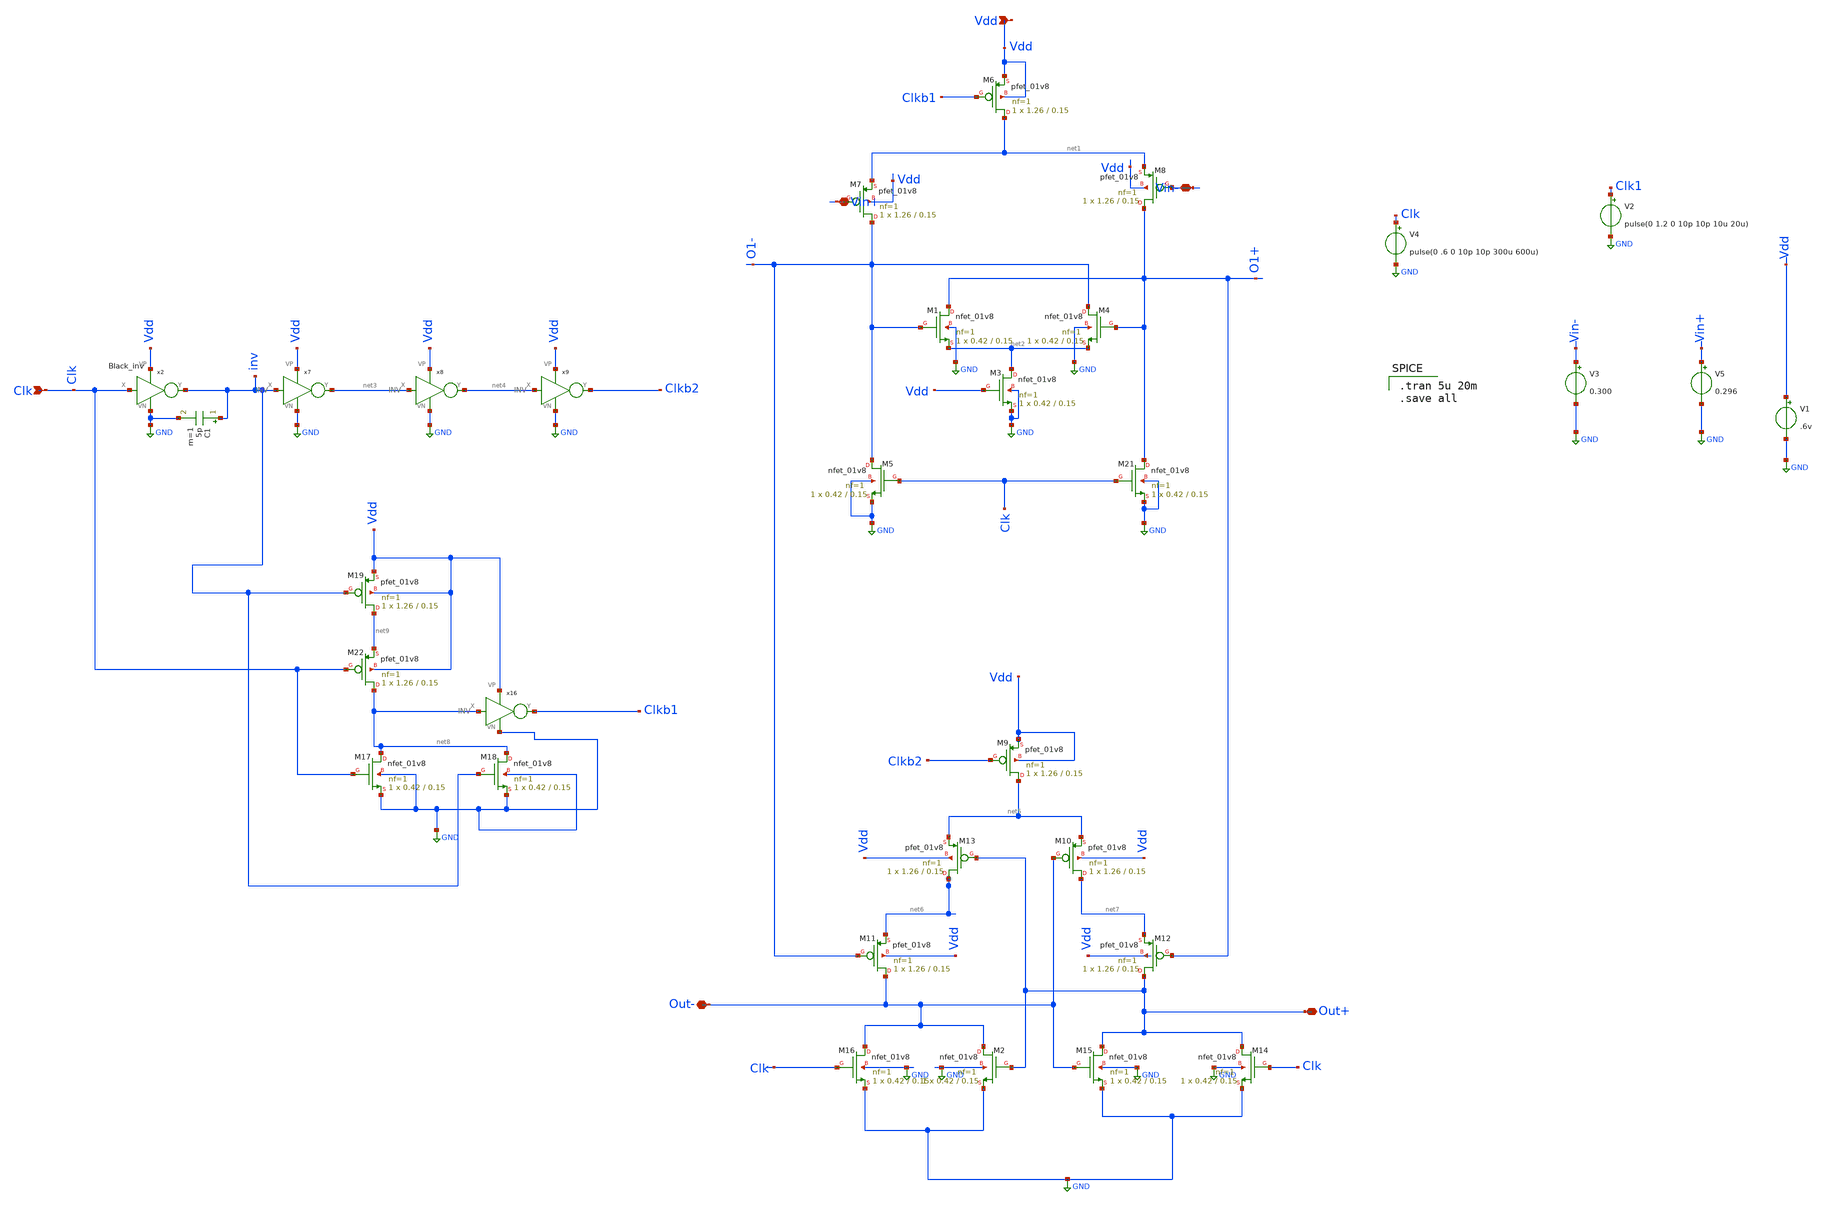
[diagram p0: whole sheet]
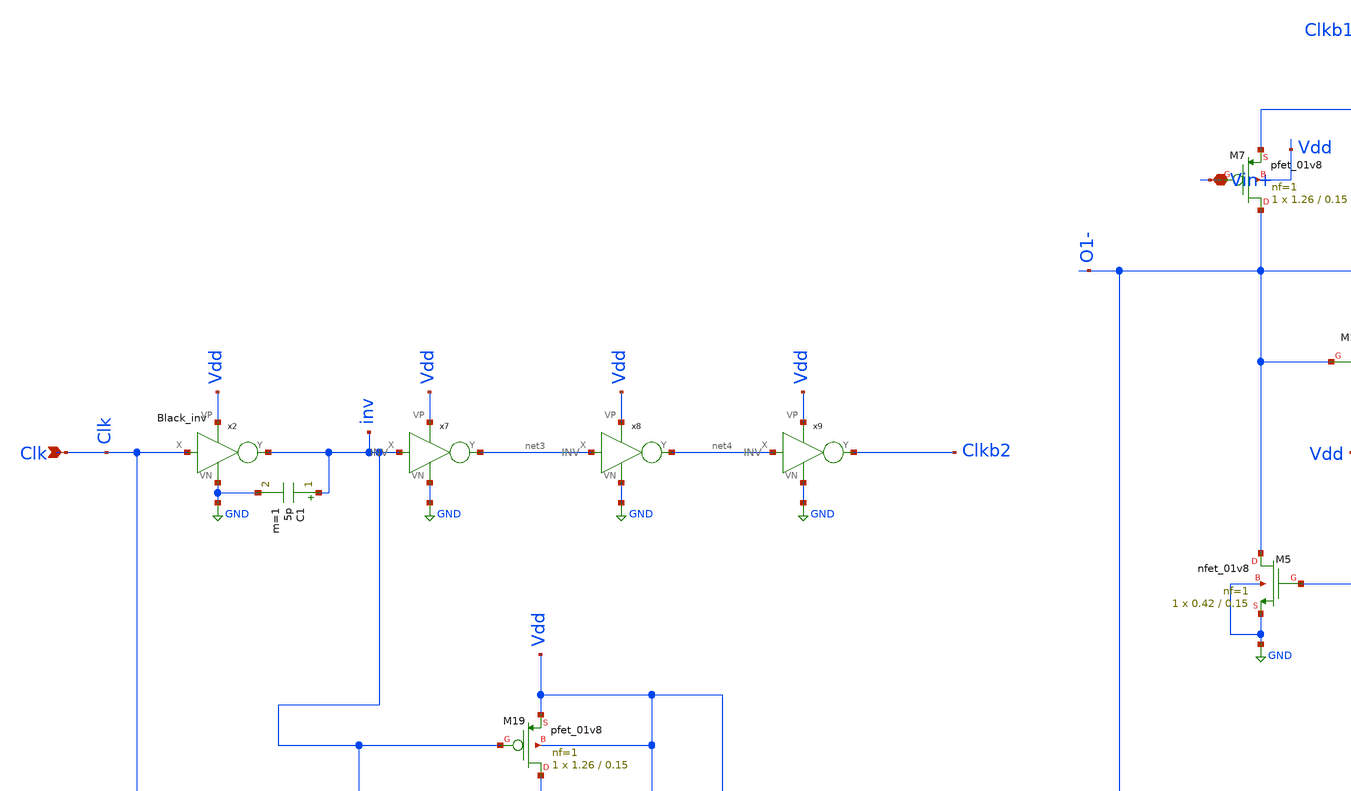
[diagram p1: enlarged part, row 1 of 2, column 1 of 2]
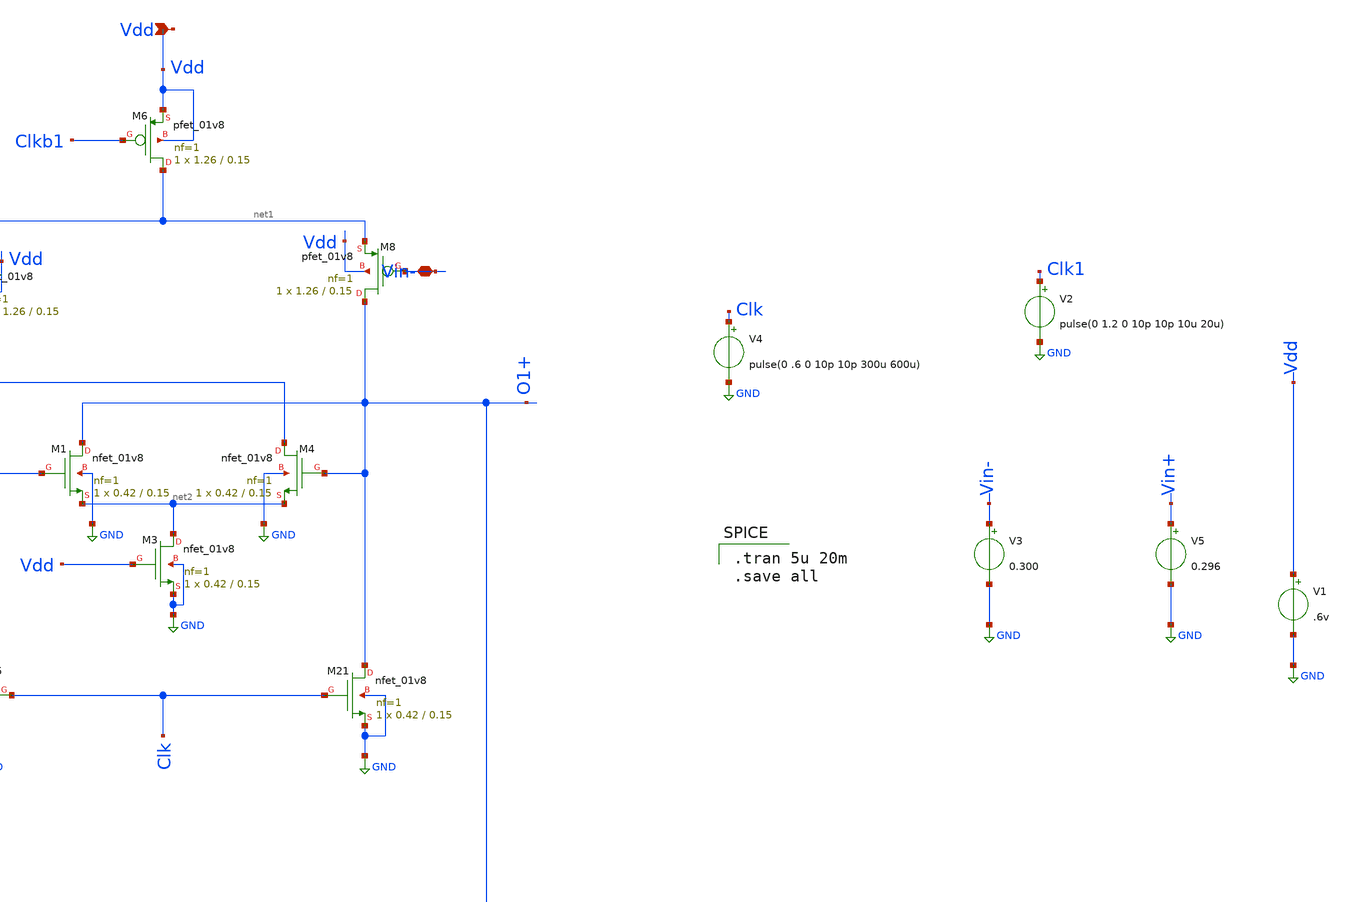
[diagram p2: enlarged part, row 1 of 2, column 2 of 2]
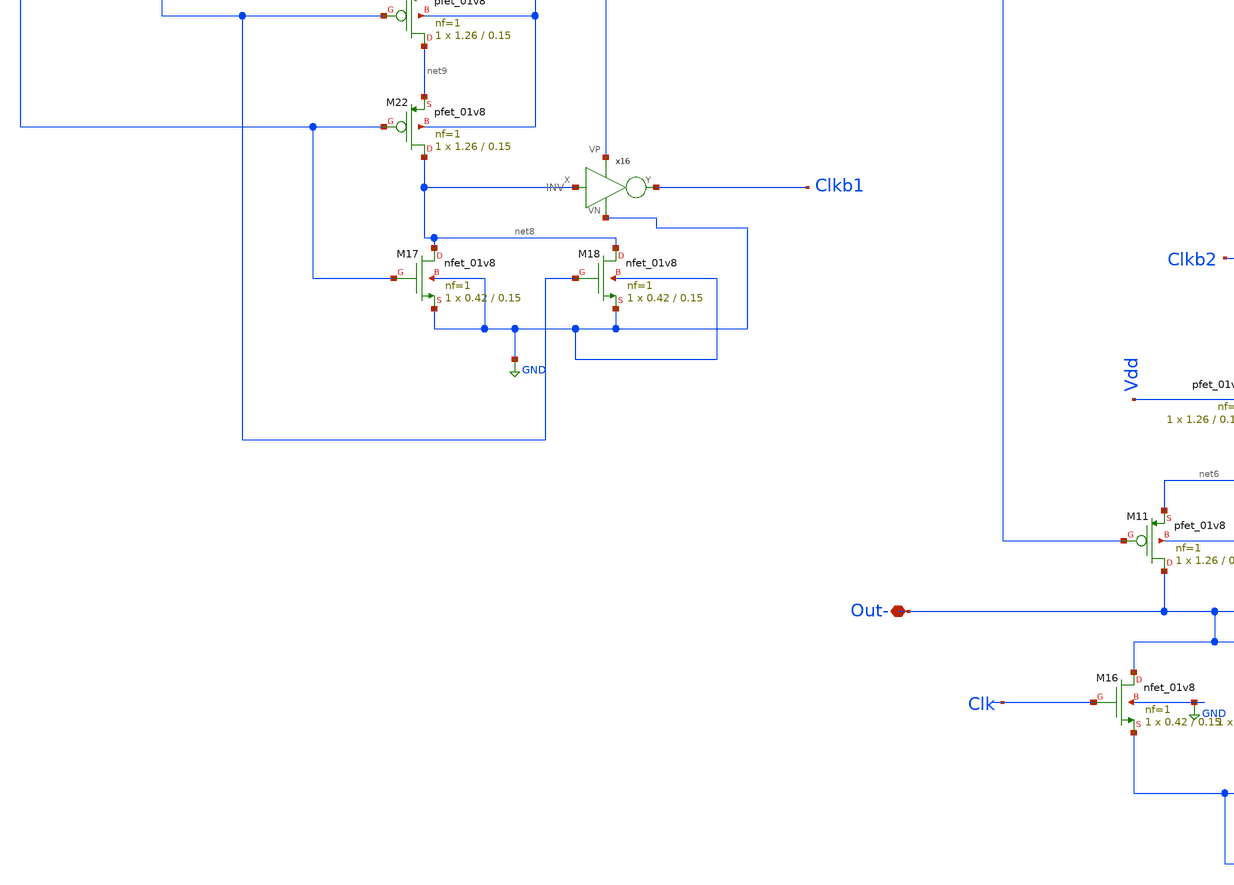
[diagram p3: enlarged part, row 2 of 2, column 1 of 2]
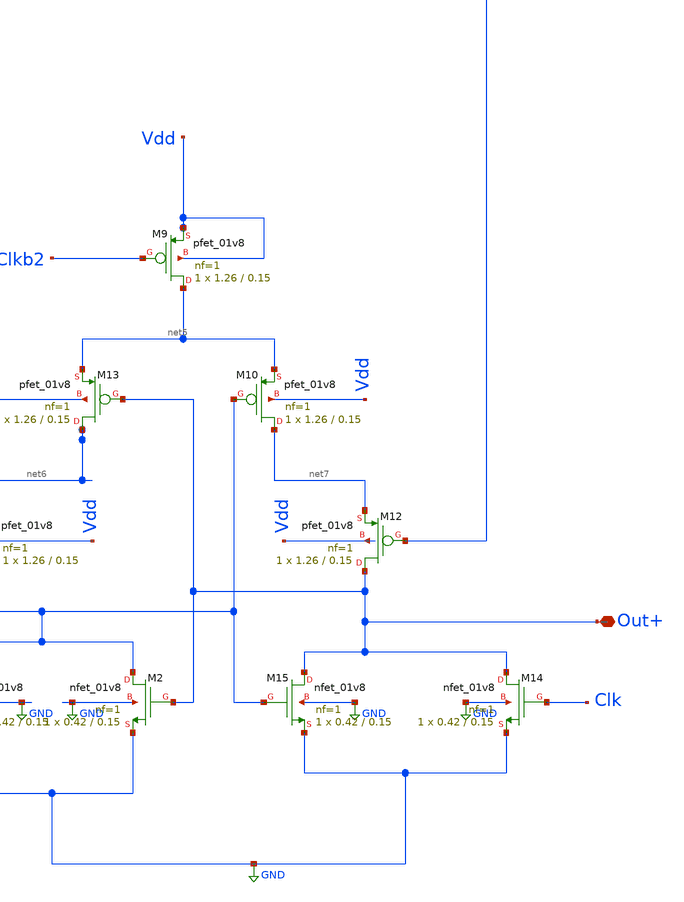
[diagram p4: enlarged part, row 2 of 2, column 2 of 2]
** sch_path: Blocks/comparator_150nm/Com_test_150_clkgen (copy).sch
**.subckt Com_test_150_clkgen (copy) Vin+ Vin- Out+ Out- Vdd Clk
*.iopin Vin+
*.iopin Vin-
*.iopin Out+
*.iopin Out-
*.ipin Vdd
*.ipin Clk
XM6 net1 Clkb1 Vdd Vdd sky130_fd_pr__pfet_01v8 L=0.15 W=1.26 nf=1 ad='int((nf+1)/2) * W/nf * 0.29' as='int((nf+2)/2) * W/nf * 0.29'
+ pd='2*int((nf+1)/2) * (W/nf + 0.29)' ps='2*int((nf+2)/2) * (W/nf + 0.29)' nrd='0.29 / W' nrs='0.29 / W'
+ sa=0 sb=0 sd=0 mult=1 m=1
XM7 O1- Vin+ net1 Vdd sky130_fd_pr__pfet_01v8 L=0.15 W=1.26 nf=1 ad='int((nf+1)/2) * W/nf * 0.29' as='int((nf+2)/2) * W/nf * 0.29'
+ pd='2*int((nf+1)/2) * (W/nf + 0.29)' ps='2*int((nf+2)/2) * (W/nf + 0.29)' nrd='0.29 / W' nrs='0.29 / W'
+ sa=0 sb=0 sd=0 mult=1 m=1
XM8 O1+ Vin- net1 Vdd sky130_fd_pr__pfet_01v8 L=0.15 W=1.26 nf=1 ad='int((nf+1)/2) * W/nf * 0.29' as='int((nf+2)/2) * W/nf * 0.29'
+ pd='2*int((nf+1)/2) * (W/nf + 0.29)' ps='2*int((nf+2)/2) * (W/nf + 0.29)' nrd='0.29 / W' nrs='0.29 / W'
+ sa=0 sb=0 sd=0 mult=1 m=1
XM9 net5 Clkb2 Vdd Vdd sky130_fd_pr__pfet_01v8 L=0.15 W=1.26 nf=1 ad='int((nf+1)/2) * W/nf * 0.29' as='int((nf+2)/2) * W/nf * 0.29'
+ pd='2*int((nf+1)/2) * (W/nf + 0.29)' ps='2*int((nf+2)/2) * (W/nf + 0.29)' nrd='0.29 / W' nrs='0.29 / W'
+ sa=0 sb=0 sd=0 mult=1 m=1
XM10 net7 Out- net5 Vdd sky130_fd_pr__pfet_01v8 L=0.15 W=1.26 nf=1 ad='int((nf+1)/2) * W/nf * 0.29' as='int((nf+2)/2) * W/nf * 0.29'
+ pd='2*int((nf+1)/2) * (W/nf + 0.29)' ps='2*int((nf+2)/2) * (W/nf + 0.29)' nrd='0.29 / W' nrs='0.29 / W'
+ sa=0 sb=0 sd=0 mult=1 m=1
XM11 Out- O1- net6 Vdd sky130_fd_pr__pfet_01v8 L=0.15 W=1.26 nf=1 ad='int((nf+1)/2) * W/nf * 0.29' as='int((nf+2)/2) * W/nf * 0.29'
+ pd='2*int((nf+1)/2) * (W/nf + 0.29)' ps='2*int((nf+2)/2) * (W/nf + 0.29)' nrd='0.29 / W' nrs='0.29 / W'
+ sa=0 sb=0 sd=0 mult=1 m=1
XM12 Out+ O1+ net7 Vdd sky130_fd_pr__pfet_01v8 L=0.15 W=1.26 nf=1 ad='int((nf+1)/2) * W/nf * 0.29' as='int((nf+2)/2) * W/nf * 0.29'
+ pd='2*int((nf+1)/2) * (W/nf + 0.29)' ps='2*int((nf+2)/2) * (W/nf + 0.29)' nrd='0.29 / W' nrs='0.29 / W'
+ sa=0 sb=0 sd=0 mult=1 m=1
XM13 net6 Out+ net5 Vdd sky130_fd_pr__pfet_01v8 L=0.15 W=1.26 nf=1 ad='int((nf+1)/2) * W/nf * 0.29' as='int((nf+2)/2) * W/nf * 0.29'
+ pd='2*int((nf+1)/2) * (W/nf + 0.29)' ps='2*int((nf+2)/2) * (W/nf + 0.29)' nrd='0.29 / W' nrs='0.29 / W'
+ sa=0 sb=0 sd=0 mult=1 m=1
XM1 O1+ O1- net2 GND sky130_fd_pr__nfet_01v8 L=0.15 W=0.42 nf=1 ad='int((nf+1)/2) * W/nf * 0.29' as='int((nf+2)/2) * W/nf * 0.29'
+ pd='2*int((nf+1)/2) * (W/nf + 0.29)' ps='2*int((nf+2)/2) * (W/nf + 0.29)' nrd='0.29 / W' nrs='0.29 / W'
+ sa=0 sb=0 sd=0 mult=1 m=1
XM3 net2 Vdd GND GND sky130_fd_pr__nfet_01v8 L=0.15 W=0.42 nf=1 ad='int((nf+1)/2) * W/nf * 0.29' as='int((nf+2)/2) * W/nf * 0.29'
+ pd='2*int((nf+1)/2) * (W/nf + 0.29)' ps='2*int((nf+2)/2) * (W/nf + 0.29)' nrd='0.29 / W' nrs='0.29 / W'
+ sa=0 sb=0 sd=0 mult=1 m=1
XM4 O1- O1+ net2 GND sky130_fd_pr__nfet_01v8 L=0.15 W=0.42 nf=1 ad='int((nf+1)/2) * W/nf * 0.29' as='int((nf+2)/2) * W/nf * 0.29'
+ pd='2*int((nf+1)/2) * (W/nf + 0.29)' ps='2*int((nf+2)/2) * (W/nf + 0.29)' nrd='0.29 / W' nrs='0.29 / W'
+ sa=0 sb=0 sd=0 mult=1 m=1
XM5 O1- Clk GND GND sky130_fd_pr__nfet_01v8 L=0.15 W=0.42 nf=1 ad='int((nf+1)/2) * W/nf * 0.29' as='int((nf+2)/2) * W/nf * 0.29'
+ pd='2*int((nf+1)/2) * (W/nf + 0.29)' ps='2*int((nf+2)/2) * (W/nf + 0.29)' nrd='0.29 / W' nrs='0.29 / W'
+ sa=0 sb=0 sd=0 mult=1 m=1
XM21 O1+ Clk GND GND sky130_fd_pr__nfet_01v8 L=0.15 W=0.42 nf=1 ad='int((nf+1)/2) * W/nf * 0.29' as='int((nf+2)/2) * W/nf * 0.29'
+ pd='2*int((nf+1)/2) * (W/nf + 0.29)' ps='2*int((nf+2)/2) * (W/nf + 0.29)' nrd='0.29 / W' nrs='0.29 / W'
+ sa=0 sb=0 sd=0 mult=1 m=1
XM2 Out- Out+ GND GND sky130_fd_pr__nfet_01v8 L=0.15 W=0.42 nf=1 ad='int((nf+1)/2) * W/nf * 0.29' as='int((nf+2)/2) * W/nf * 0.29'
+ pd='2*int((nf+1)/2) * (W/nf + 0.29)' ps='2*int((nf+2)/2) * (W/nf + 0.29)' nrd='0.29 / W' nrs='0.29 / W'
+ sa=0 sb=0 sd=0 mult=1 m=1
XM14 Out+ Clk GND GND sky130_fd_pr__nfet_01v8 L=0.15 W=0.42 nf=1 ad='int((nf+1)/2) * W/nf * 0.29' as='int((nf+2)/2) * W/nf * 0.29'
+ pd='2*int((nf+1)/2) * (W/nf + 0.29)' ps='2*int((nf+2)/2) * (W/nf + 0.29)' nrd='0.29 / W' nrs='0.29 / W'
+ sa=0 sb=0 sd=0 mult=1 m=1
XM15 Out+ Out- GND GND sky130_fd_pr__nfet_01v8 L=0.15 W=0.42 nf=1 ad='int((nf+1)/2) * W/nf * 0.29' as='int((nf+2)/2) * W/nf * 0.29'
+ pd='2*int((nf+1)/2) * (W/nf + 0.29)' ps='2*int((nf+2)/2) * (W/nf + 0.29)' nrd='0.29 / W' nrs='0.29 / W'
+ sa=0 sb=0 sd=0 mult=1 m=1
XM16 Out- Clk GND GND sky130_fd_pr__nfet_01v8 L=0.15 W=0.42 nf=1 ad='int((nf+1)/2) * W/nf * 0.29' as='int((nf+2)/2) * W/nf * 0.29'
+ pd='2*int((nf+1)/2) * (W/nf + 0.29)' ps='2*int((nf+2)/2) * (W/nf + 0.29)' nrd='0.29 / W' nrs='0.29 / W'
+ sa=0 sb=0 sd=0 mult=1 m=1
XM17 net8 Clk GND GND sky130_fd_pr__nfet_01v8 L=0.15 W=0.42 nf=1 ad='int((nf+1)/2) * W/nf * 0.29' as='int((nf+2)/2) * W/nf * 0.29'
+ pd='2*int((nf+1)/2) * (W/nf + 0.29)' ps='2*int((nf+2)/2) * (W/nf + 0.29)' nrd='0.29 / W' nrs='0.29 / W'
+ sa=0 sb=0 sd=0 mult=1 m=1
XM18 net8 inv GND GND sky130_fd_pr__nfet_01v8 L=0.15 W=0.42 nf=1 ad='int((nf+1)/2) * W/nf * 0.29' as='int((nf+2)/2) * W/nf * 0.29'
+ pd='2*int((nf+1)/2) * (W/nf + 0.29)' ps='2*int((nf+2)/2) * (W/nf + 0.29)' nrd='0.29 / W' nrs='0.29 / W'
+ sa=0 sb=0 sd=0 mult=1 m=1
XM19 net9 inv Vdd Vdd sky130_fd_pr__pfet_01v8 L=0.15 W=1.26 nf=1 ad='int((nf+1)/2) * W/nf * 0.29' as='int((nf+2)/2) * W/nf * 0.29'
+ pd='2*int((nf+1)/2) * (W/nf + 0.29)' ps='2*int((nf+2)/2) * (W/nf + 0.29)' nrd='0.29 / W' nrs='0.29 / W'
+ sa=0 sb=0 sd=0 mult=1 m=1
XM22 net8 Clk net9 Vdd sky130_fd_pr__pfet_01v8 L=0.15 W=1.26 nf=1 ad='int((nf+1)/2) * W/nf * 0.29' as='int((nf+2)/2) * W/nf * 0.29'
+ pd='2*int((nf+1)/2) * (W/nf + 0.29)' ps='2*int((nf+2)/2) * (W/nf + 0.29)' nrd='0.29 / W' nrs='0.29 / W'
+ sa=0 sb=0 sd=0 mult=1 m=1
x2 Clk inv Vdd GND black_inv
x7 inv net3 Vdd GND INV
x8 net3 net4 Vdd GND INV
x9 net4 Clkb2 Vdd GND INV
x16 net8 Clkb1 Vdd GND INV
V3 Vin- GND 0.300
V5 Vin+ GND 0.296
V1 Vdd GND .6v
V2 Clk1 GND pulse(0 1.2 0 10p 10p 10u 20u)
V4 Clk GND pulse(0 .6 0 10p 10p 300u 600u)
C1 inv GND 5p m=1
**** begin user architecture code

** opencircuitdesign pdks install
.lib $::SKYWATER_MODELS/sky130.lib.spice tt



.tran 5u 20m
.save all

**** end user architecture code
**.ends

* expanding   symbol:  component/black_inv_1/black_inv.sym # of pins=4
** sym_path: component/black_inv_1/black_inv.sym
** sch_path: component/black_inv_1/black_inv.sch
.subckt black_inv X Y VP VN
*.ipin X
*.opin Y
*.iopin VN
*.iopin VP
XM8 Y X VP VP sky130_fd_pr__pfet_01v8 L=.18 W=1.59 nf=1 ad='int((nf+1)/2) * W/nf * 0.29' as='int((nf+2)/2) * W/nf * 0.29'
+ pd='2*int((nf+1)/2) * (W/nf + 0.29)' ps='2*int((nf+2)/2) * (W/nf + 0.29)' nrd='0.29 / W' nrs='0.29 / W'
+ sa=0 sb=0 sd=0 mult=1 m=1
XM4 Y X VN VN sky130_fd_pr__nfet_01v8 L=0.18 W=0.502 nf=1 ad='int((nf+1)/2) * W/nf * 0.29' as='int((nf+2)/2) * W/nf * 0.29'
+ pd='2*int((nf+1)/2) * (W/nf + 0.29)' ps='2*int((nf+2)/2) * (W/nf + 0.29)' nrd='0.29 / W' nrs='0.29 / W'
+ sa=0 sb=0 sd=0 mult=1 m=1
.ends


* expanding   symbol:  component/Inverter/INV.sym # of pins=4
** sym_path: component/Inverter/INV.sym
** sch_path: component/Inverter/INV.sch
.subckt INV X Y VP VN
*.ipin X
*.opin Y
*.iopin VN
*.iopin VP
XM8 Y X VP VP sky130_fd_pr__pfet_01v8 L=.18 W=1.512 nf=1 ad='int((nf+1)/2) * W/nf * 0.29' as='int((nf+2)/2) * W/nf * 0.29'
+ pd='2*int((nf+1)/2) * (W/nf + 0.29)' ps='2*int((nf+2)/2) * (W/nf + 0.29)' nrd='0.29 / W' nrs='0.29 / W'
+ sa=0 sb=0 sd=0 mult=1 m=1
XM4 Y X VN VN sky130_fd_pr__nfet_01v8 L=0.18 W=0.42 nf=1 ad='int((nf+1)/2) * W/nf * 0.29' as='int((nf+2)/2) * W/nf * 0.29'
+ pd='2*int((nf+1)/2) * (W/nf + 0.29)' ps='2*int((nf+2)/2) * (W/nf + 0.29)' nrd='0.29 / W' nrs='0.29 / W'
+ sa=0 sb=0 sd=0 mult=1 m=1
.ends

.GLOBAL GND
.end
